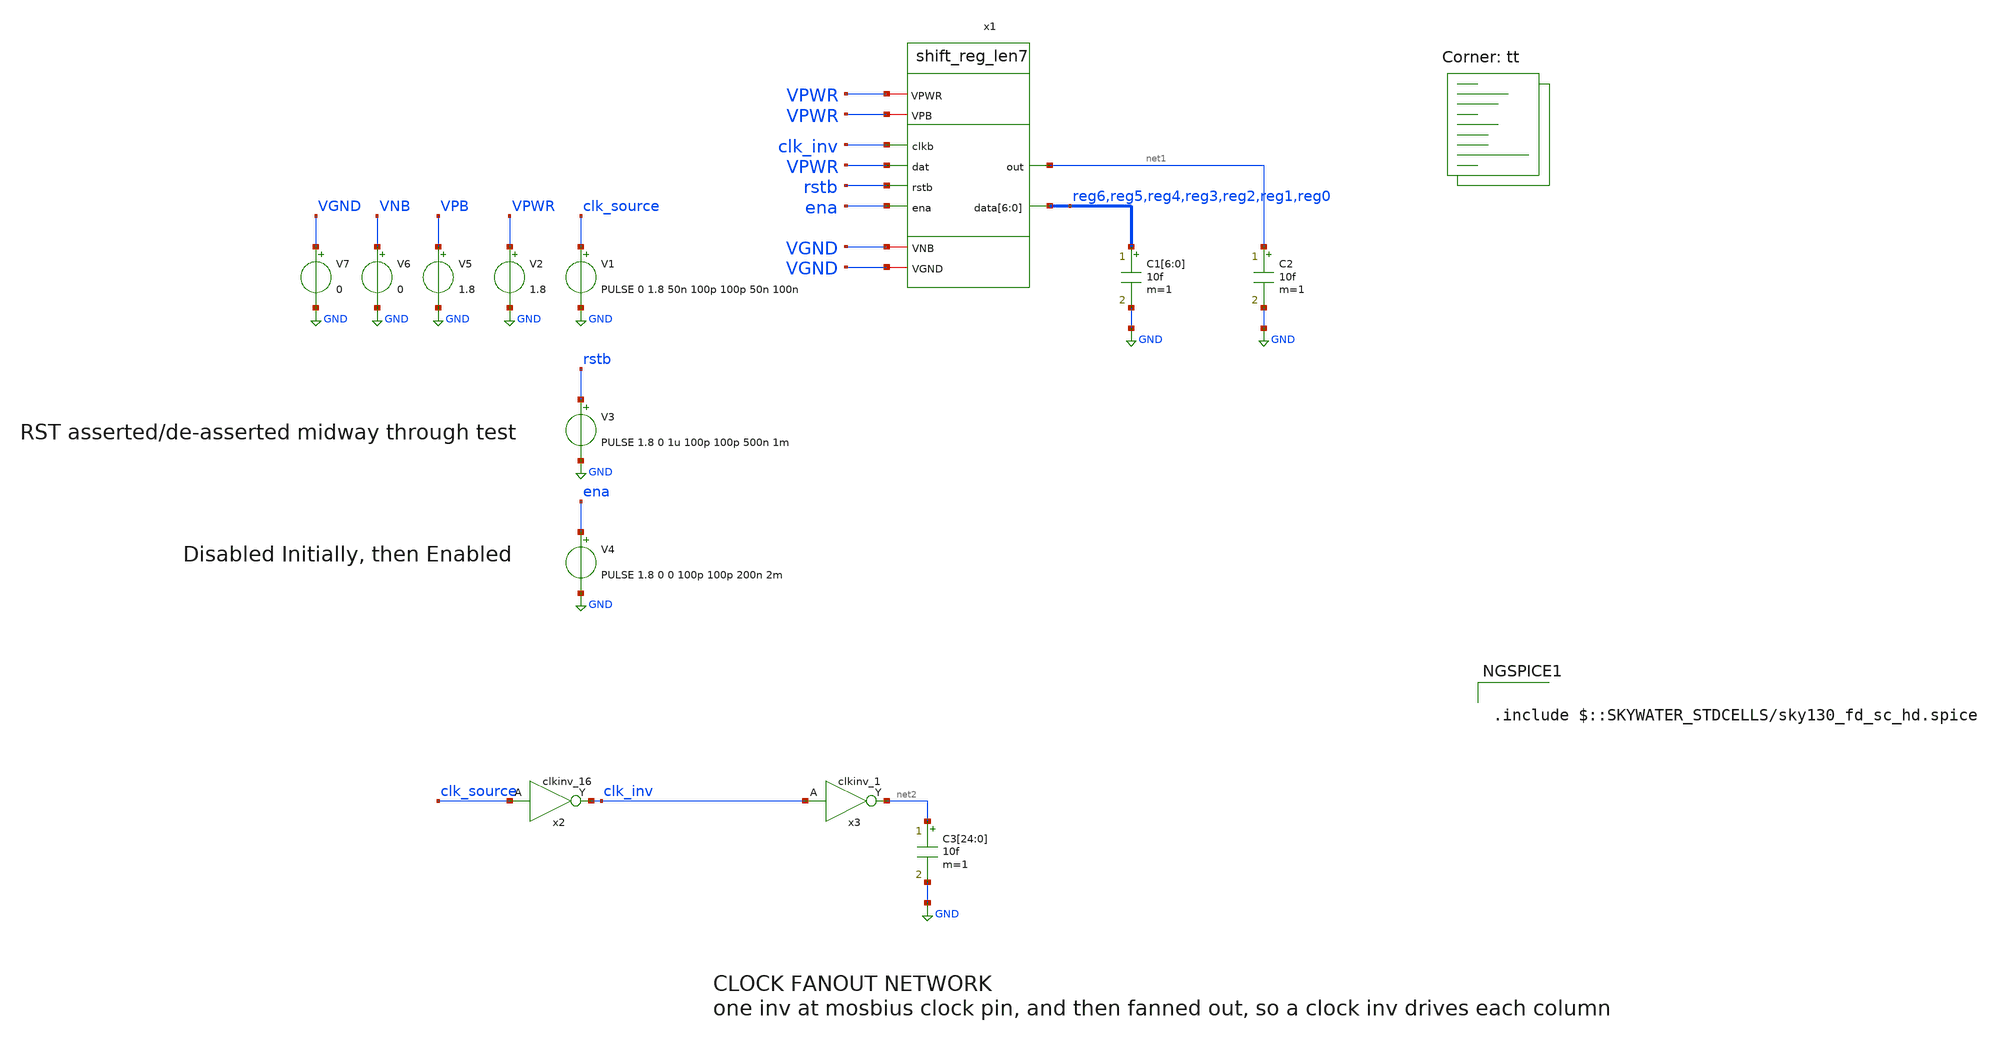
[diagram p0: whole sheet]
** sch_path: tt_um_mosbius/xschem/tb_shift_reg.sch
**.subckt tb_shift_reg
V2 VPWR GND 1.8
C1[6] reg6 GND 10f m=1
C1[5] reg5 GND 10f m=1
C1[4] reg4 GND 10f m=1
C1[3] reg3 GND 10f m=1
C1[2] reg2 GND 10f m=1
C1[1] reg1 GND 10f m=1
C1[0] reg0 GND 10f m=1
V1 clk_source GND PULSE 0 1.8 50n 100p 100p 50n 100n
V3 rstb GND PULSE 1.8 0 1u 100p 100p 500n 1m
V4 ena GND PULSE 1.8 0 0 100p 100p 200n 2m
C2 net1 GND 10f m=1
x2 clk_source VGND VNB VPB VPWR clk_inv sky130_fd_sc_hd__clkinv_16
x3 clk_inv VGND VNB VPB VPWR net2 sky130_fd_sc_hd__clkinv_1
C3[24] net2 GND 10f m=1
C3[23] net2 GND 10f m=1
C3[22] net2 GND 10f m=1
C3[21] net2 GND 10f m=1
C3[20] net2 GND 10f m=1
C3[19] net2 GND 10f m=1
C3[18] net2 GND 10f m=1
C3[17] net2 GND 10f m=1
C3[16] net2 GND 10f m=1
C3[15] net2 GND 10f m=1
C3[14] net2 GND 10f m=1
C3[13] net2 GND 10f m=1
C3[12] net2 GND 10f m=1
C3[11] net2 GND 10f m=1
C3[10] net2 GND 10f m=1
C3[9] net2 GND 10f m=1
C3[8] net2 GND 10f m=1
C3[7] net2 GND 10f m=1
C3[6] net2 GND 10f m=1
C3[5] net2 GND 10f m=1
C3[4] net2 GND 10f m=1
C3[3] net2 GND 10f m=1
C3[2] net2 GND 10f m=1
C3[1] net2 GND 10f m=1
C3[0] net2 GND 10f m=1
V5 VPB GND 1.8
V6 VNB GND 0
V7 VGND GND 0
x1 VPWR net1 clk_inv VPWR rstb ena VGND reg6 reg5 reg4 reg3 reg2 reg1 reg0 VPWR VGND shift_reg_len7
**** begin user architecture code
.lib $::SKYWATER_MODELS/sky130.lib.spice tt


*****************************************
* Shift Register Test
*****************************************
* holds a logic 1 at the shift reg input, and it propagates down
* the shift register. A asynchronous reset is also asserted.
* a shorter 8-bit shift register is tested for simulation time.
* includes clock fanout network
*****************************************
.control
   save all
   set temp=27
   tran 100p 3u
   plot v(reg0) v(reg1) v(reg2) v(reg3) v(reg4) v(reg5) v(reg6)
   plot v(rstb) v(ena)
   plot v(clk_source) v(clk_inv)
.endc



.include $::SKYWATER_STDCELLS/sky130_fd_sc_hd.spice

**** end user architecture code
**.ends

* expanding   symbol:  shift_reg_len7.sym # of pins=10
** sym_path: tt_um_mosbius/xschem/shift_reg_len7.sym
** sch_path: tt_um_mosbius/xschem/shift_reg_len7.sch
.subckt shift_reg_len7 VPWR out clkb dat rstb ena VGND data[6] data[5] data[4] data[3] data[2]
+ data[1] data[0] VPB VNB
*.ipin clkb
*.ipin dat
*.ipin rstb
*.iopin VPWR
*.iopin VGND
*.opin data[6],data[5],data[4],data[3],data[2],data[1],data[0]
*.ipin ena
*.opin out
*.iopin VPB
*.iopin VNB
x8 clkb VGND VNB VPB VPWR clk sky130_fd_sc_hd__clkinv_1
x9[6] out ena VGND VNB VPB VPWR data[6] sky130_fd_sc_hd__and2_1
x9[5] reg[5] ena VGND VNB VPB VPWR data[5] sky130_fd_sc_hd__and2_1
x9[4] reg[4] ena VGND VNB VPB VPWR data[4] sky130_fd_sc_hd__and2_1
x9[3] reg[3] ena VGND VNB VPB VPWR data[3] sky130_fd_sc_hd__and2_1
x9[2] reg[2] ena VGND VNB VPB VPWR data[2] sky130_fd_sc_hd__and2_1
x9[1] reg[1] ena VGND VNB VPB VPWR data[1] sky130_fd_sc_hd__and2_1
x9[0] reg[0] ena VGND VNB VPB VPWR data[0] sky130_fd_sc_hd__and2_1
x1 clk dat rstb VGND VNB VPB VPWR reg[0] sky130_fd_sc_hd__dfrtp_1
x2 clk reg[0] rstb VGND VNB VPB VPWR reg[1] sky130_fd_sc_hd__dfrtp_1
x3 clk reg[1] rstb VGND VNB VPB VPWR reg[2] sky130_fd_sc_hd__dfrtp_1
x4 clk reg[2] rstb VGND VNB VPB VPWR reg[3] sky130_fd_sc_hd__dfrtp_1
x5 clk reg[3] rstb VGND VNB VPB VPWR reg[4] sky130_fd_sc_hd__dfrtp_1
x6 clk reg[4] rstb VGND VNB VPB VPWR reg[5] sky130_fd_sc_hd__dfrtp_1
x7 clk reg[5] rstb VGND VNB VPB VPWR out sky130_fd_sc_hd__dfrtp_1
.ends

.GLOBAL GND
.end
